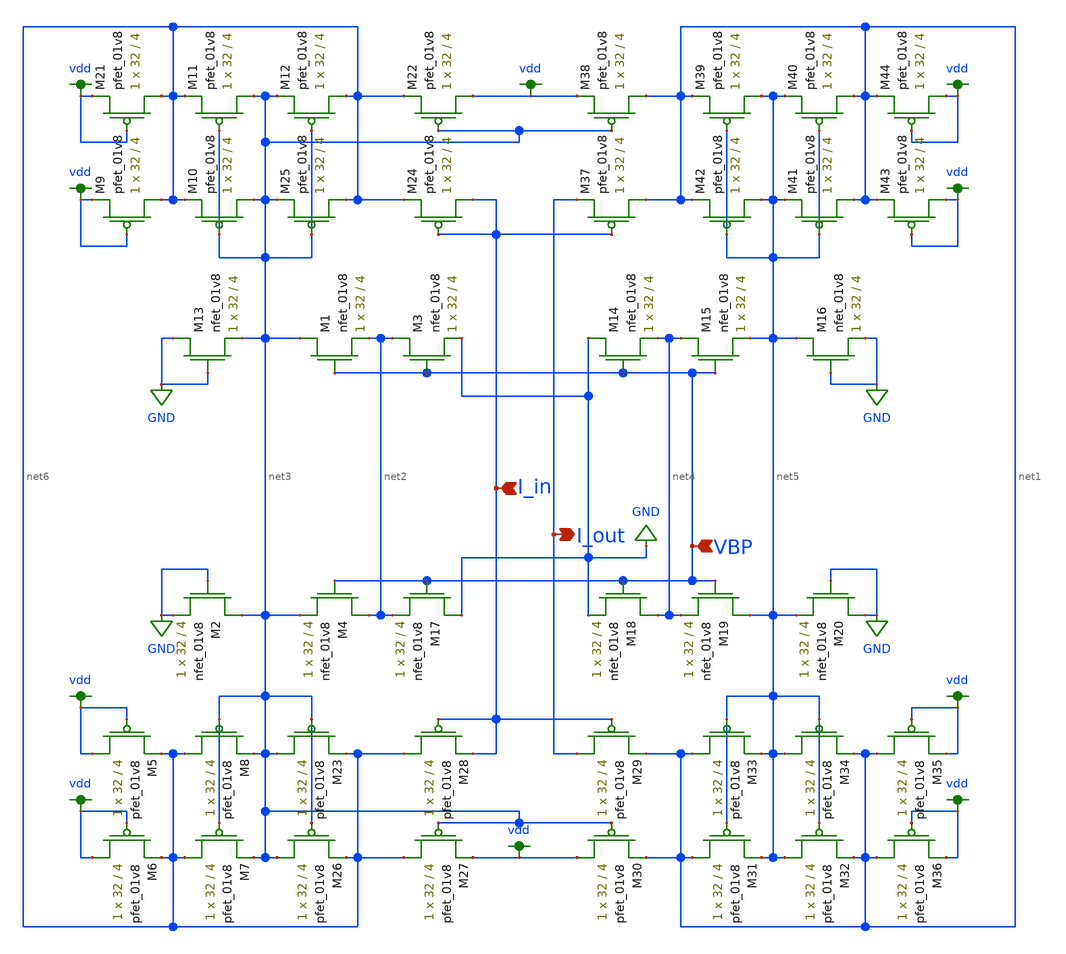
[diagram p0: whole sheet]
** sch_path: schemas/LDS_first_current_mirror.sch
**.subckt LDS_first_current_mirror I_out VBP I_in
*.opin I_out
*.ipin VBP
*.ipin I_in
XM13 GND GND net3 GND sky130_fd_pr__nfet_01v8 L=4 W=32 nf=1 ad='int((nf+1)/2) * W/nf * 0.29' as='int((nf+2)/2) * W/nf * 0.29'
+ pd='2*int((nf+1)/2) * (W/nf + 0.29)' ps='2*int((nf+2)/2) * (W/nf + 0.29)' nrd='0.29 / W' nrs='0.29 / W'
+ sa=0 sb=0 sd=0 mult=1 m=1
XM1 net3 VBP net2 GND sky130_fd_pr__nfet_01v8 L=4 W=32 nf=1 ad='int((nf+1)/2) * W/nf * 0.29' as='int((nf+2)/2) * W/nf * 0.29'
+ pd='2*int((nf+1)/2) * (W/nf + 0.29)' ps='2*int((nf+2)/2) * (W/nf + 0.29)' nrd='0.29 / W' nrs='0.29 / W'
+ sa=0 sb=0 sd=0 mult=1 m=1
XM3 net2 VBP GND GND sky130_fd_pr__nfet_01v8 L=4 W=32 nf=1 ad='int((nf+1)/2) * W/nf * 0.29' as='int((nf+2)/2) * W/nf * 0.29'
+ pd='2*int((nf+1)/2) * (W/nf + 0.29)' ps='2*int((nf+2)/2) * (W/nf + 0.29)' nrd='0.29 / W' nrs='0.29 / W'
+ sa=0 sb=0 sd=0 mult=1 m=1
XM14 GND VBP net4 GND sky130_fd_pr__nfet_01v8 L=4 W=32 nf=1 ad='int((nf+1)/2) * W/nf * 0.29' as='int((nf+2)/2) * W/nf * 0.29'
+ pd='2*int((nf+1)/2) * (W/nf + 0.29)' ps='2*int((nf+2)/2) * (W/nf + 0.29)' nrd='0.29 / W' nrs='0.29 / W'
+ sa=0 sb=0 sd=0 mult=1 m=1
XM15 net4 VBP net5 GND sky130_fd_pr__nfet_01v8 L=4 W=32 nf=1 ad='int((nf+1)/2) * W/nf * 0.29' as='int((nf+2)/2) * W/nf * 0.29'
+ pd='2*int((nf+1)/2) * (W/nf + 0.29)' ps='2*int((nf+2)/2) * (W/nf + 0.29)' nrd='0.29 / W' nrs='0.29 / W'
+ sa=0 sb=0 sd=0 mult=1 m=1
XM16 net5 GND GND GND sky130_fd_pr__nfet_01v8 L=4 W=32 nf=1 ad='int((nf+1)/2) * W/nf * 0.29' as='int((nf+2)/2) * W/nf * 0.29'
+ pd='2*int((nf+1)/2) * (W/nf + 0.29)' ps='2*int((nf+2)/2) * (W/nf + 0.29)' nrd='0.29 / W' nrs='0.29 / W'
+ sa=0 sb=0 sd=0 mult=1 m=1
XM2 net3 GND GND GND sky130_fd_pr__nfet_01v8 L=4 W=32 nf=1 ad='int((nf+1)/2) * W/nf * 0.29' as='int((nf+2)/2) * W/nf * 0.29'
+ pd='2*int((nf+1)/2) * (W/nf + 0.29)' ps='2*int((nf+2)/2) * (W/nf + 0.29)' nrd='0.29 / W' nrs='0.29 / W'
+ sa=0 sb=0 sd=0 mult=1 m=1
XM4 net2 VBP net3 GND sky130_fd_pr__nfet_01v8 L=4 W=32 nf=1 ad='int((nf+1)/2) * W/nf * 0.29' as='int((nf+2)/2) * W/nf * 0.29'
+ pd='2*int((nf+1)/2) * (W/nf + 0.29)' ps='2*int((nf+2)/2) * (W/nf + 0.29)' nrd='0.29 / W' nrs='0.29 / W'
+ sa=0 sb=0 sd=0 mult=1 m=1
XM17 GND VBP net2 GND sky130_fd_pr__nfet_01v8 L=4 W=32 nf=1 ad='int((nf+1)/2) * W/nf * 0.29' as='int((nf+2)/2) * W/nf * 0.29'
+ pd='2*int((nf+1)/2) * (W/nf + 0.29)' ps='2*int((nf+2)/2) * (W/nf + 0.29)' nrd='0.29 / W' nrs='0.29 / W'
+ sa=0 sb=0 sd=0 mult=1 m=1
XM18 net4 VBP GND GND sky130_fd_pr__nfet_01v8 L=4 W=32 nf=1 ad='int((nf+1)/2) * W/nf * 0.29' as='int((nf+2)/2) * W/nf * 0.29'
+ pd='2*int((nf+1)/2) * (W/nf + 0.29)' ps='2*int((nf+2)/2) * (W/nf + 0.29)' nrd='0.29 / W' nrs='0.29 / W'
+ sa=0 sb=0 sd=0 mult=1 m=1
XM19 net5 VBP net4 GND sky130_fd_pr__nfet_01v8 L=4 W=32 nf=1 ad='int((nf+1)/2) * W/nf * 0.29' as='int((nf+2)/2) * W/nf * 0.29'
+ pd='2*int((nf+1)/2) * (W/nf + 0.29)' ps='2*int((nf+2)/2) * (W/nf + 0.29)' nrd='0.29 / W' nrs='0.29 / W'
+ sa=0 sb=0 sd=0 mult=1 m=1
XM20 GND GND net5 GND sky130_fd_pr__nfet_01v8 L=4 W=32 nf=1 ad='int((nf+1)/2) * W/nf * 0.29' as='int((nf+2)/2) * W/nf * 0.29'
+ pd='2*int((nf+1)/2) * (W/nf + 0.29)' ps='2*int((nf+2)/2) * (W/nf + 0.29)' nrd='0.29 / W' nrs='0.29 / W'
+ sa=0 sb=0 sd=0 mult=1 m=1
XM21 net6 vdd vdd VDD sky130_fd_pr__pfet_01v8 L=4 W=32 nf=1 ad='int((nf+1)/2) * W/nf * 0.29' as='int((nf+2)/2) * W/nf * 0.29'
+ pd='2*int((nf+1)/2) * (W/nf + 0.29)' ps='2*int((nf+2)/2) * (W/nf + 0.29)' nrd='0.29 / W' nrs='0.29 / W'
+ sa=0 sb=0 sd=0 mult=1 m=1
XM9 net6 vdd vdd VDD sky130_fd_pr__pfet_01v8 L=4 W=32 nf=1 ad='int((nf+1)/2) * W/nf * 0.29' as='int((nf+2)/2) * W/nf * 0.29'
+ pd='2*int((nf+1)/2) * (W/nf + 0.29)' ps='2*int((nf+2)/2) * (W/nf + 0.29)' nrd='0.29 / W' nrs='0.29 / W'
+ sa=0 sb=0 sd=0 mult=1 m=1
XM10 net3 net3 net6 VDD sky130_fd_pr__pfet_01v8 L=4 W=32 nf=1 ad='int((nf+1)/2) * W/nf * 0.29' as='int((nf+2)/2) * W/nf * 0.29'
+ pd='2*int((nf+1)/2) * (W/nf + 0.29)' ps='2*int((nf+2)/2) * (W/nf + 0.29)' nrd='0.29 / W' nrs='0.29 / W'
+ sa=0 sb=0 sd=0 mult=1 m=1
XM11 net3 net3 net6 VDD sky130_fd_pr__pfet_01v8 L=4 W=32 nf=1 ad='int((nf+1)/2) * W/nf * 0.29' as='int((nf+2)/2) * W/nf * 0.29'
+ pd='2*int((nf+1)/2) * (W/nf + 0.29)' ps='2*int((nf+2)/2) * (W/nf + 0.29)' nrd='0.29 / W' nrs='0.29 / W'
+ sa=0 sb=0 sd=0 mult=1 m=1
XM12 net6 net3 net3 VDD sky130_fd_pr__pfet_01v8 L=4 W=32 nf=1 ad='int((nf+1)/2) * W/nf * 0.29' as='int((nf+2)/2) * W/nf * 0.29'
+ pd='2*int((nf+1)/2) * (W/nf + 0.29)' ps='2*int((nf+2)/2) * (W/nf + 0.29)' nrd='0.29 / W' nrs='0.29 / W'
+ sa=0 sb=0 sd=0 mult=1 m=1
XM22 vdd net3 net6 VDD sky130_fd_pr__pfet_01v8 L=4 W=32 nf=1 ad='int((nf+1)/2) * W/nf * 0.29' as='int((nf+2)/2) * W/nf * 0.29'
+ pd='2*int((nf+1)/2) * (W/nf + 0.29)' ps='2*int((nf+2)/2) * (W/nf + 0.29)' nrd='0.29 / W' nrs='0.29 / W'
+ sa=0 sb=0 sd=0 mult=1 m=1
XM24 I_in I_in net6 VDD sky130_fd_pr__pfet_01v8 L=4 W=32 nf=1 ad='int((nf+1)/2) * W/nf * 0.29' as='int((nf+2)/2) * W/nf * 0.29'
+ pd='2*int((nf+1)/2) * (W/nf + 0.29)' ps='2*int((nf+2)/2) * (W/nf + 0.29)' nrd='0.29 / W' nrs='0.29 / W'
+ sa=0 sb=0 sd=0 mult=1 m=1
XM25 net6 net3 net3 VDD sky130_fd_pr__pfet_01v8 L=4 W=32 nf=1 ad='int((nf+1)/2) * W/nf * 0.29' as='int((nf+2)/2) * W/nf * 0.29'
+ pd='2*int((nf+1)/2) * (W/nf + 0.29)' ps='2*int((nf+2)/2) * (W/nf + 0.29)' nrd='0.29 / W' nrs='0.29 / W'
+ sa=0 sb=0 sd=0 mult=1 m=1
XM37 net1 I_in I_out VDD sky130_fd_pr__pfet_01v8 L=4 W=32 nf=1 ad='int((nf+1)/2) * W/nf * 0.29' as='int((nf+2)/2) * W/nf * 0.29'
+ pd='2*int((nf+1)/2) * (W/nf + 0.29)' ps='2*int((nf+2)/2) * (W/nf + 0.29)' nrd='0.29 / W' nrs='0.29 / W'
+ sa=0 sb=0 sd=0 mult=1 m=1
XM38 net1 net3 vdd VDD sky130_fd_pr__pfet_01v8 L=4 W=32 nf=1 ad='int((nf+1)/2) * W/nf * 0.29' as='int((nf+2)/2) * W/nf * 0.29'
+ pd='2*int((nf+1)/2) * (W/nf + 0.29)' ps='2*int((nf+2)/2) * (W/nf + 0.29)' nrd='0.29 / W' nrs='0.29 / W'
+ sa=0 sb=0 sd=0 mult=1 m=1
XM39 net5 net5 net1 VDD sky130_fd_pr__pfet_01v8 L=4 W=32 nf=1 ad='int((nf+1)/2) * W/nf * 0.29' as='int((nf+2)/2) * W/nf * 0.29'
+ pd='2*int((nf+1)/2) * (W/nf + 0.29)' ps='2*int((nf+2)/2) * (W/nf + 0.29)' nrd='0.29 / W' nrs='0.29 / W'
+ sa=0 sb=0 sd=0 mult=1 m=1
XM40 net1 net5 net5 VDD sky130_fd_pr__pfet_01v8 L=4 W=32 nf=1 ad='int((nf+1)/2) * W/nf * 0.29' as='int((nf+2)/2) * W/nf * 0.29'
+ pd='2*int((nf+1)/2) * (W/nf + 0.29)' ps='2*int((nf+2)/2) * (W/nf + 0.29)' nrd='0.29 / W' nrs='0.29 / W'
+ sa=0 sb=0 sd=0 mult=1 m=1
XM41 net1 net5 net5 VDD sky130_fd_pr__pfet_01v8 L=4 W=32 nf=1 ad='int((nf+1)/2) * W/nf * 0.29' as='int((nf+2)/2) * W/nf * 0.29'
+ pd='2*int((nf+1)/2) * (W/nf + 0.29)' ps='2*int((nf+2)/2) * (W/nf + 0.29)' nrd='0.29 / W' nrs='0.29 / W'
+ sa=0 sb=0 sd=0 mult=1 m=1
XM42 net5 net5 net1 VDD sky130_fd_pr__pfet_01v8 L=4 W=32 nf=1 ad='int((nf+1)/2) * W/nf * 0.29' as='int((nf+2)/2) * W/nf * 0.29'
+ pd='2*int((nf+1)/2) * (W/nf + 0.29)' ps='2*int((nf+2)/2) * (W/nf + 0.29)' nrd='0.29 / W' nrs='0.29 / W'
+ sa=0 sb=0 sd=0 mult=1 m=1
XM43 vdd vdd net1 VDD sky130_fd_pr__pfet_01v8 L=4 W=32 nf=1 ad='int((nf+1)/2) * W/nf * 0.29' as='int((nf+2)/2) * W/nf * 0.29'
+ pd='2*int((nf+1)/2) * (W/nf + 0.29)' ps='2*int((nf+2)/2) * (W/nf + 0.29)' nrd='0.29 / W' nrs='0.29 / W'
+ sa=0 sb=0 sd=0 mult=1 m=1
XM44 vdd vdd net1 VDD sky130_fd_pr__pfet_01v8 L=4 W=32 nf=1 ad='int((nf+1)/2) * W/nf * 0.29' as='int((nf+2)/2) * W/nf * 0.29'
+ pd='2*int((nf+1)/2) * (W/nf + 0.29)' ps='2*int((nf+2)/2) * (W/nf + 0.29)' nrd='0.29 / W' nrs='0.29 / W'
+ sa=0 sb=0 sd=0 mult=1 m=1
XM5 vdd vdd net6 VDD sky130_fd_pr__pfet_01v8 L=4 W=32 nf=1 ad='int((nf+1)/2) * W/nf * 0.29' as='int((nf+2)/2) * W/nf * 0.29'
+ pd='2*int((nf+1)/2) * (W/nf + 0.29)' ps='2*int((nf+2)/2) * (W/nf + 0.29)' nrd='0.29 / W' nrs='0.29 / W'
+ sa=0 sb=0 sd=0 mult=1 m=1
XM6 vdd vdd net6 VDD sky130_fd_pr__pfet_01v8 L=4 W=32 nf=1 ad='int((nf+1)/2) * W/nf * 0.29' as='int((nf+2)/2) * W/nf * 0.29'
+ pd='2*int((nf+1)/2) * (W/nf + 0.29)' ps='2*int((nf+2)/2) * (W/nf + 0.29)' nrd='0.29 / W' nrs='0.29 / W'
+ sa=0 sb=0 sd=0 mult=1 m=1
XM7 net6 net3 net3 VDD sky130_fd_pr__pfet_01v8 L=4 W=32 nf=1 ad='int((nf+1)/2) * W/nf * 0.29' as='int((nf+2)/2) * W/nf * 0.29'
+ pd='2*int((nf+1)/2) * (W/nf + 0.29)' ps='2*int((nf+2)/2) * (W/nf + 0.29)' nrd='0.29 / W' nrs='0.29 / W'
+ sa=0 sb=0 sd=0 mult=1 m=1
XM8 net6 net3 net3 VDD sky130_fd_pr__pfet_01v8 L=4 W=32 nf=1 ad='int((nf+1)/2) * W/nf * 0.29' as='int((nf+2)/2) * W/nf * 0.29'
+ pd='2*int((nf+1)/2) * (W/nf + 0.29)' ps='2*int((nf+2)/2) * (W/nf + 0.29)' nrd='0.29 / W' nrs='0.29 / W'
+ sa=0 sb=0 sd=0 mult=1 m=1
XM23 net3 net3 net6 VDD sky130_fd_pr__pfet_01v8 L=4 W=32 nf=1 ad='int((nf+1)/2) * W/nf * 0.29' as='int((nf+2)/2) * W/nf * 0.29'
+ pd='2*int((nf+1)/2) * (W/nf + 0.29)' ps='2*int((nf+2)/2) * (W/nf + 0.29)' nrd='0.29 / W' nrs='0.29 / W'
+ sa=0 sb=0 sd=0 mult=1 m=1
XM26 net3 net3 net6 VDD sky130_fd_pr__pfet_01v8 L=4 W=32 nf=1 ad='int((nf+1)/2) * W/nf * 0.29' as='int((nf+2)/2) * W/nf * 0.29'
+ pd='2*int((nf+1)/2) * (W/nf + 0.29)' ps='2*int((nf+2)/2) * (W/nf + 0.29)' nrd='0.29 / W' nrs='0.29 / W'
+ sa=0 sb=0 sd=0 mult=1 m=1
XM27 net6 net3 vdd VDD sky130_fd_pr__pfet_01v8 L=4 W=32 nf=1 ad='int((nf+1)/2) * W/nf * 0.29' as='int((nf+2)/2) * W/nf * 0.29'
+ pd='2*int((nf+1)/2) * (W/nf + 0.29)' ps='2*int((nf+2)/2) * (W/nf + 0.29)' nrd='0.29 / W' nrs='0.29 / W'
+ sa=0 sb=0 sd=0 mult=1 m=1
XM28 net6 I_in I_in VDD sky130_fd_pr__pfet_01v8 L=4 W=32 nf=1 ad='int((nf+1)/2) * W/nf * 0.29' as='int((nf+2)/2) * W/nf * 0.29'
+ pd='2*int((nf+1)/2) * (W/nf + 0.29)' ps='2*int((nf+2)/2) * (W/nf + 0.29)' nrd='0.29 / W' nrs='0.29 / W'
+ sa=0 sb=0 sd=0 mult=1 m=1
XM29 I_out I_in net1 VDD sky130_fd_pr__pfet_01v8 L=4 W=32 nf=1 ad='int((nf+1)/2) * W/nf * 0.29' as='int((nf+2)/2) * W/nf * 0.29'
+ pd='2*int((nf+1)/2) * (W/nf + 0.29)' ps='2*int((nf+2)/2) * (W/nf + 0.29)' nrd='0.29 / W' nrs='0.29 / W'
+ sa=0 sb=0 sd=0 mult=1 m=1
XM30 vdd net3 net1 VDD sky130_fd_pr__pfet_01v8 L=4 W=32 nf=1 ad='int((nf+1)/2) * W/nf * 0.29' as='int((nf+2)/2) * W/nf * 0.29'
+ pd='2*int((nf+1)/2) * (W/nf + 0.29)' ps='2*int((nf+2)/2) * (W/nf + 0.29)' nrd='0.29 / W' nrs='0.29 / W'
+ sa=0 sb=0 sd=0 mult=1 m=1
XM31 net1 net5 net5 VDD sky130_fd_pr__pfet_01v8 L=4 W=32 nf=1 ad='int((nf+1)/2) * W/nf * 0.29' as='int((nf+2)/2) * W/nf * 0.29'
+ pd='2*int((nf+1)/2) * (W/nf + 0.29)' ps='2*int((nf+2)/2) * (W/nf + 0.29)' nrd='0.29 / W' nrs='0.29 / W'
+ sa=0 sb=0 sd=0 mult=1 m=1
XM32 net5 net5 net1 VDD sky130_fd_pr__pfet_01v8 L=4 W=32 nf=1 ad='int((nf+1)/2) * W/nf * 0.29' as='int((nf+2)/2) * W/nf * 0.29'
+ pd='2*int((nf+1)/2) * (W/nf + 0.29)' ps='2*int((nf+2)/2) * (W/nf + 0.29)' nrd='0.29 / W' nrs='0.29 / W'
+ sa=0 sb=0 sd=0 mult=1 m=1
XM33 net1 net5 net5 VDD sky130_fd_pr__pfet_01v8 L=4 W=32 nf=1 ad='int((nf+1)/2) * W/nf * 0.29' as='int((nf+2)/2) * W/nf * 0.29'
+ pd='2*int((nf+1)/2) * (W/nf + 0.29)' ps='2*int((nf+2)/2) * (W/nf + 0.29)' nrd='0.29 / W' nrs='0.29 / W'
+ sa=0 sb=0 sd=0 mult=1 m=1
XM34 net5 net5 net1 VDD sky130_fd_pr__pfet_01v8 L=4 W=32 nf=1 ad='int((nf+1)/2) * W/nf * 0.29' as='int((nf+2)/2) * W/nf * 0.29'
+ pd='2*int((nf+1)/2) * (W/nf + 0.29)' ps='2*int((nf+2)/2) * (W/nf + 0.29)' nrd='0.29 / W' nrs='0.29 / W'
+ sa=0 sb=0 sd=0 mult=1 m=1
XM35 net1 vdd vdd VDD sky130_fd_pr__pfet_01v8 L=4 W=32 nf=1 ad='int((nf+1)/2) * W/nf * 0.29' as='int((nf+2)/2) * W/nf * 0.29'
+ pd='2*int((nf+1)/2) * (W/nf + 0.29)' ps='2*int((nf+2)/2) * (W/nf + 0.29)' nrd='0.29 / W' nrs='0.29 / W'
+ sa=0 sb=0 sd=0 mult=1 m=1
XM36 net1 vdd vdd VDD sky130_fd_pr__pfet_01v8 L=4 W=32 nf=1 ad='int((nf+1)/2) * W/nf * 0.29' as='int((nf+2)/2) * W/nf * 0.29'
+ pd='2*int((nf+1)/2) * (W/nf + 0.29)' ps='2*int((nf+2)/2) * (W/nf + 0.29)' nrd='0.29 / W' nrs='0.29 / W'
+ sa=0 sb=0 sd=0 mult=1 m=1
**.ends
.GLOBAL vdd
.GLOBAL GND
.end
